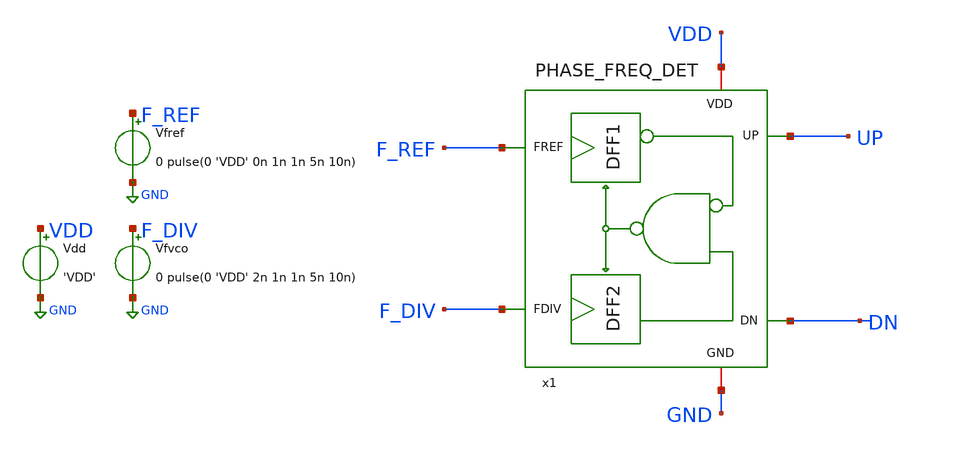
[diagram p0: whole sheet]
** sch_path: xschem/phase-freq-detector/tb_PHASE_FREQ_DET_PEX.sch
**.subckt tb_PHASE_FREQ_DET_PEX
Vdd VDD GND 'VDD'
Vfvco F_DIV GND 0 pulse(0 'VDD' 2n 1n 1n 5n 10n)
Vfref F_REF GND 0 pulse(0 'VDD' 0n 1n 1n 5n 10n)
x1 F_REF UP VDD GND F_DIV DN PHASE_FREQ_DET_PEX
**** begin user architecture code



.lib cornerMOSlv.lib mos_tt
.lib cornerMOShv.lib mos_tt
.lib cornerHBT.lib hbt_typ
.lib cornerRES.lib res_typ
.include /foss/pdks/ihp-sg13g2/libs.ref/sg13g2_stdcell/spice/sg13g2_stdcell.spice
.global VDD GND







* Nominal conditions (27 C, 1.2 V). For the Monte Carlo spread of temperature and supply
* used in the paper, replace them by:
*   .param RAW_TEMP = agauss(40, 30, 1)
*   .param TEMPGAUSS = max(20, min(RAW_TEMP, 80))
*   .option temp = 'TEMPGAUSS'
*   .param VDDGAUSS = agauss(1.2, 0.05, 1)
*   .param VDD = 'VDDGAUSS'
.option temp = 27
.include /foss/designs/unicasss-tools/SG13G2_2.4GHz_LC_VCO_FPLL/pex/PHASE_FREQ_DET__PHASE_FREQ_DET/magic_RC/PHASE_FREQ_DET.pex.spice
.param VDD = 1.2
* analysis

.tran 100p 30n uic

.control
run
write tb_PHASE_FREQ_DET_PEX.raw
meas tran up_avg avg v(UP) from=10n to=30n
meas tran dn_avg avg v(DN) from=10n to=30n
meas tran up_r2 when v(UP)=0.6 rise=2
meas tran up_f2 when v(UP)=0.6 fall=2
meas tran dn_r2 when v(DN)=0.6 rise=2
meas tran dn_f2 when v(DN)=0.6 fall=2
* supply current (negative = drawn from the source), power = 1.2 V x |idd|
meas tran idd avg i(Vdd) from=10n to=30n
plot v(F_REF) v(F_DIV)
plot v(UP) v(DN)
.endc



**** end user architecture code
**.ends
.GLOBAL GND
.end
